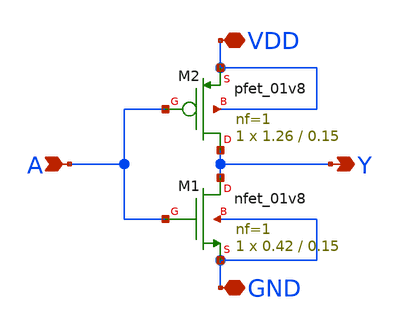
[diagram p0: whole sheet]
** sch_path: cells/INV1X1/schematic/inv1x1.sch
**.subckt inv1x1 A Y VDD GND
*.ipin A
*.opin Y
*.iopin VDD
*.iopin GND
XM1 Y A GND GND sky130_fd_pr__nfet_01v8 L=0.15 W=0.42 nf=1 ad='int((1 + 1)/2) * 0.42 / 1 * 0.29' as='int((1 + 2)/2) * 0.42 / 1 * 0.29'
+ pd='2*int((1 + 1)/2) * (0.42 / 1 + 0.29)' ps='2*int((1 + 2)/2) * (0.42 / 1 + 0.29)' nrd='0.29 / 0.42 '
+ nrs='0.29 / 0.42 ' sa=0 sb=0 sd=0 mult=1 m=1
XM2 Y A VDD VDD sky130_fd_pr__pfet_01v8 L=0.15 W=1.26 nf=1 ad='int((1 + 1)/2) * 1.26 / 1 * 0.29' as='int((1 + 2)/2) * 1.26 / 1 * 0.29'
+ pd='2*int((1 + 1)/2) * (1.26 / 1 + 0.29)' ps='2*int((1 + 2)/2) * (1.26 / 1 + 0.29)' nrd='0.29 / 1.26 '
+ nrs='0.29 / 1.26 ' sa=0 sb=0 sd=0 mult=1 m=1
**.ends
.end
